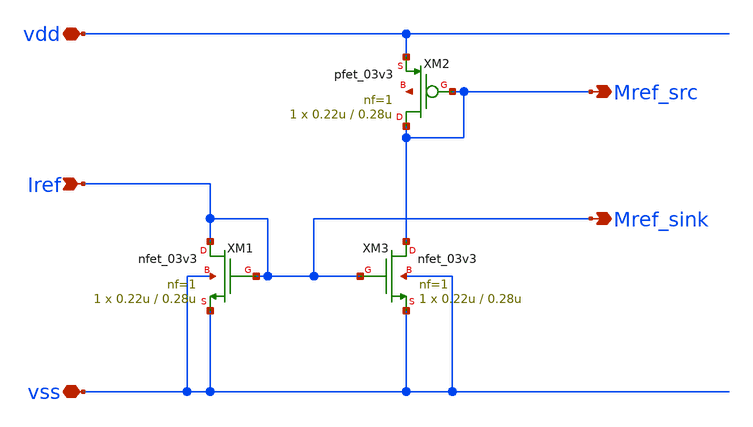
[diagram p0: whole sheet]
** sch_path: designs/libs/core_analog/iref/iref.sch
**.subckt iref Iref vdd vss Mref_src Mref_sink
*.ipin Iref
*.iopin vdd
*.iopin vss
*.opin Mref_src
*.opin Mref_sink
XM1 Iref Iref vss vss nfet_03v3 L=0.28u W=0.22u nf=1 ad='int((nf+1)/2) * W/nf * 0.18u' as='int((nf+2)/2) * W/nf * 0.18u'
+ pd='2*int((nf+1)/2) * (W/nf + 0.18u)' ps='2*int((nf+2)/2) * (W/nf + 0.18u)' nrd='0.18u / W' nrs='0.18u / W'
+ sa=0 sb=0 sd=0 m=1
XM2 Mref_src Mref_src vdd net1 pfet_03v3 L=0.28u W=0.22u nf=1 ad='int((nf+1)/2) * W/nf * 0.18u' as='int((nf+2)/2) * W/nf * 0.18u'
+ pd='2*int((nf+1)/2) * (W/nf + 0.18u)' ps='2*int((nf+2)/2) * (W/nf + 0.18u)' nrd='0.18u / W' nrs='0.18u / W'
+ sa=0 sb=0 sd=0 m=1
XM3 Mref_src Iref vss vss nfet_03v3 L=0.28u W=0.22u nf=1 ad='int((nf+1)/2) * W/nf * 0.18u' as='int((nf+2)/2) * W/nf * 0.18u'
+ pd='2*int((nf+1)/2) * (W/nf + 0.18u)' ps='2*int((nf+2)/2) * (W/nf + 0.18u)' nrd='0.18u / W' nrs='0.18u / W'
+ sa=0 sb=0 sd=0 m=1
**.ends
.end
